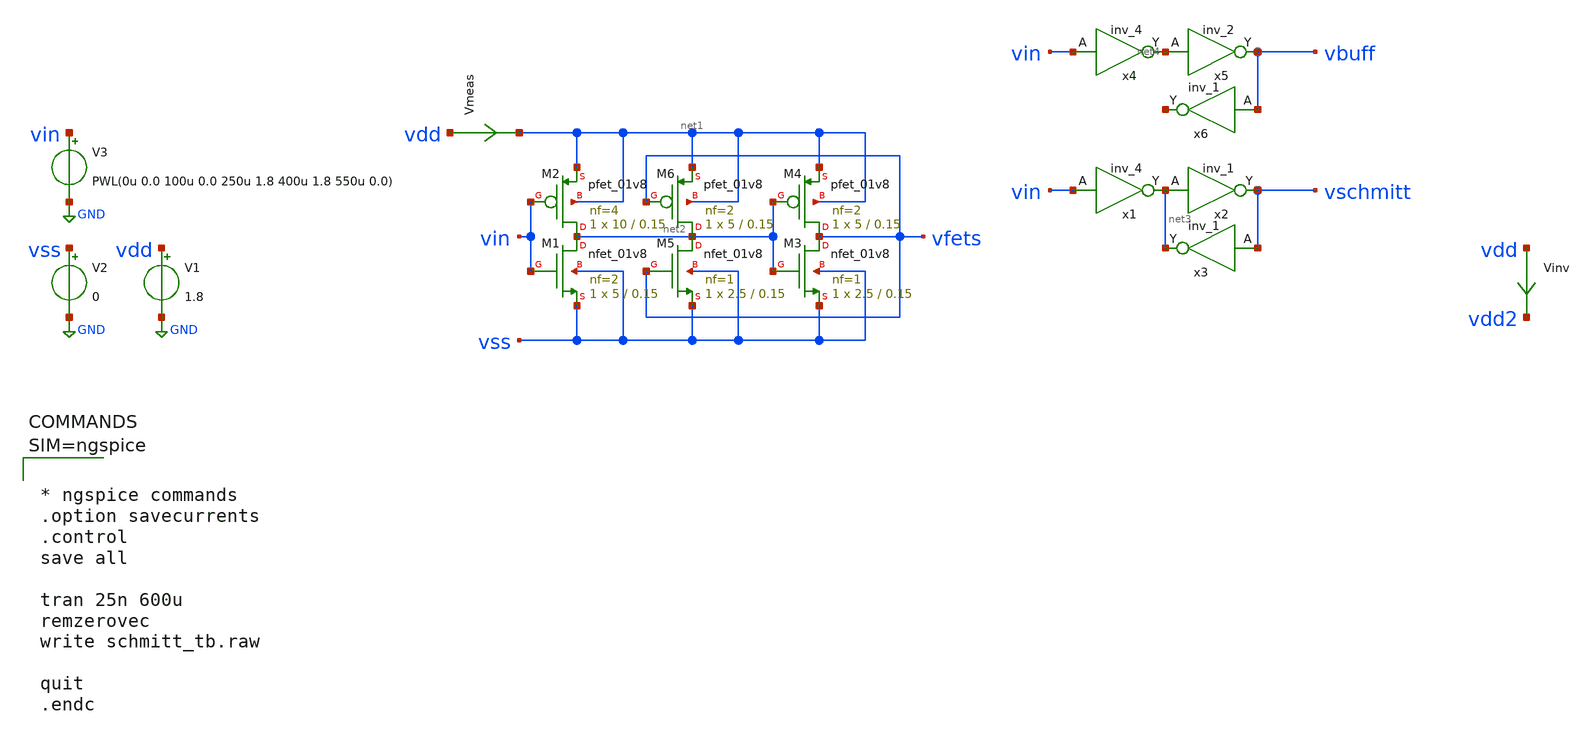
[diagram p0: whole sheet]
** sch_path: xschem/schmitt_tb.sch
**.subckt schmitt_tb
V1 vdd GND 1.8
V2 vss GND 0
V3 vin GND PWL(0u 0.0 100u 0.0 250u 1.8 400u 1.8 550u 0.0)
x1 vin vss vss vdd2 vdd2 net3 sky130_fd_sc_hd__inv_4
x2 net3 vss vss vdd2 vdd2 vschmitt sky130_fd_sc_hd__inv_1
x3 vschmitt vss vss vdd2 vdd2 net3 sky130_fd_sc_hd__inv_1
XM1 net2 vin vss vss sky130_fd_pr__nfet_01v8 L=0.15 W=5 nf=2 ad='int((nf+1)/2) * W/nf * 0.29' as='int((nf+2)/2) * W/nf * 0.29'
+ pd='2*int((nf+1)/2) * (W/nf + 0.29)' ps='2*int((nf+2)/2) * (W/nf + 0.29)' nrd='0.29 / W' nrs='0.29 / W'
+ sa=0 sb=0 sd=0 mult=1 m=1
XM2 net2 vin net1 net1 sky130_fd_pr__pfet_01v8 L=0.15 W=10 nf=4 ad='int((nf+1)/2) * W/nf * 0.29' as='int((nf+2)/2) * W/nf * 0.29'
+ pd='2*int((nf+1)/2) * (W/nf + 0.29)' ps='2*int((nf+2)/2) * (W/nf + 0.29)' nrd='0.29 / W' nrs='0.29 / W'
+ sa=0 sb=0 sd=0 mult=1 m=1
XM3 vfets net2 vss vss sky130_fd_pr__nfet_01v8 L=0.15 W=2.5 nf=1 ad='int((nf+1)/2) * W/nf * 0.29' as='int((nf+2)/2) * W/nf * 0.29'
+ pd='2*int((nf+1)/2) * (W/nf + 0.29)' ps='2*int((nf+2)/2) * (W/nf + 0.29)' nrd='0.29 / W' nrs='0.29 / W'
+ sa=0 sb=0 sd=0 mult=1 m=1
XM4 vfets net2 net1 net1 sky130_fd_pr__pfet_01v8 L=0.15 W=5 nf=2 ad='int((nf+1)/2) * W/nf * 0.29' as='int((nf+2)/2) * W/nf * 0.29'
+ pd='2*int((nf+1)/2) * (W/nf + 0.29)' ps='2*int((nf+2)/2) * (W/nf + 0.29)' nrd='0.29 / W' nrs='0.29 / W'
+ sa=0 sb=0 sd=0 mult=1 m=1
XM5 net2 vfets vss vss sky130_fd_pr__nfet_01v8 L=0.15 W=2.5 nf=1 ad='int((nf+1)/2) * W/nf * 0.29' as='int((nf+2)/2) * W/nf * 0.29'
+ pd='2*int((nf+1)/2) * (W/nf + 0.29)' ps='2*int((nf+2)/2) * (W/nf + 0.29)' nrd='0.29 / W' nrs='0.29 / W'
+ sa=0 sb=0 sd=0 mult=1 m=1
XM6 net2 vfets net1 net1 sky130_fd_pr__pfet_01v8 L=0.15 W=5 nf=2 ad='int((nf+1)/2) * W/nf * 0.29' as='int((nf+2)/2) * W/nf * 0.29'
+ pd='2*int((nf+1)/2) * (W/nf + 0.29)' ps='2*int((nf+2)/2) * (W/nf + 0.29)' nrd='0.29 / W' nrs='0.29 / W'
+ sa=0 sb=0 sd=0 mult=1 m=1
Vmeas vdd net1 0
.save i(vmeas)
Vinv vdd vdd2 0
.save i(vinv)
x4 vin vss vss vdd2 vdd2 net4 sky130_fd_sc_hd__inv_4
x5 net4 vss vss vdd2 vdd2 vbuff sky130_fd_sc_hd__inv_2
x6 vbuff vss vss vdd2 vdd2 net5 sky130_fd_sc_hd__inv_1
**** begin user architecture code

** opencircuitdesign pdks install
.lib $::SKYWATER_MODELS/sky130.lib.spice tt
.include $::SKYWATER_STDCELLS/sky130_fd_sc_hd.spice




* ngspice commands
.option savecurrents
.control
save all

tran 25n 600u
remzerovec
write schmitt_tb.raw

quit
.endc



**** end user architecture code
**.ends
.GLOBAL GND
.end
